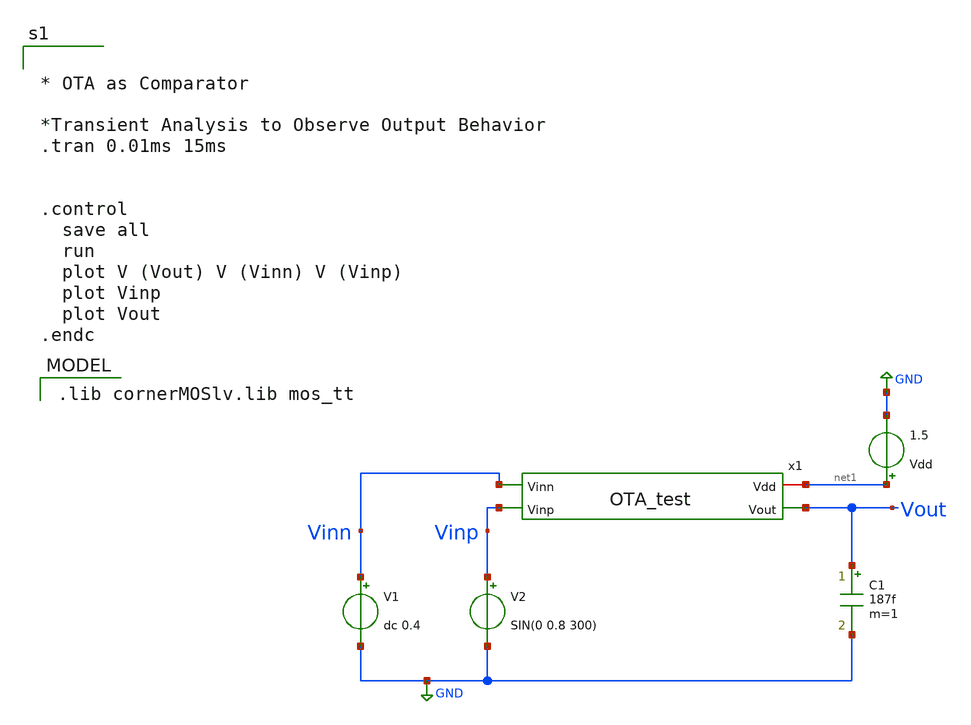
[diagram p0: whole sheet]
** sch_path: Xschem/comparator.sch
**.subckt comparator
V1 Vinn GND dc 0.4
V2 Vinp GND SIN(0 0.8 300)
Vdd net1 GND 1.5
x1 net1 Vout Vinn Vinp OTA_test
C1 Vout GND 187f m=1
**** begin user architecture code


* OTA as Comparator

*Transient Analysis to Observe Output Behavior
.tran 0.01ms 15ms


.control
  save all
  run
  plot V (Vout) V (Vinn) V (Vinp)
  plot Vinp
  plot Vout
.endc




 .lib cornerMOSlv.lib mos_tt

**** end user architecture code
**.ends

* expanding   symbol:  OTA_test.sym # of pins=4
** sym_path: Xschem/OTA_test.sym
** sch_path: Xschem/OTA_test.sch
.subckt OTA_test Vdd Vout Vinn Vinp
*.opin Vout
*.iopin Vdd
*.ipin Vinp
*.ipin Vinn
I_basis Vdd net3 20u
XM1 net1 Vinp net2 GND sg13_lv_nmos w=2u l=5u ng=1 m=1 mm_ok=1
XM5 net2 net3 GND GND sg13_lv_nmos w=0.5u l=5u ng=1 m=1 mm_ok=1
XM6 net3 net3 GND GND sg13_lv_nmos w=2.5u l=5u ng=5 m=1 mm_ok=1
XM4 Vout net1 Vdd Vdd sg13_lv_pmos w=1.5u l=5u ng=1 m=1 mm_ok=1
XM3 net1 net1 Vdd Vdd sg13_lv_pmos w=1.5u l=5u ng=1 m=1 mm_ok=1
XM2 Vout Vinn net2 GND sg13_lv_nmos w=2u l=5u ng=1 m=1 mm_ok=1
.ends

.GLOBAL GND
.end
